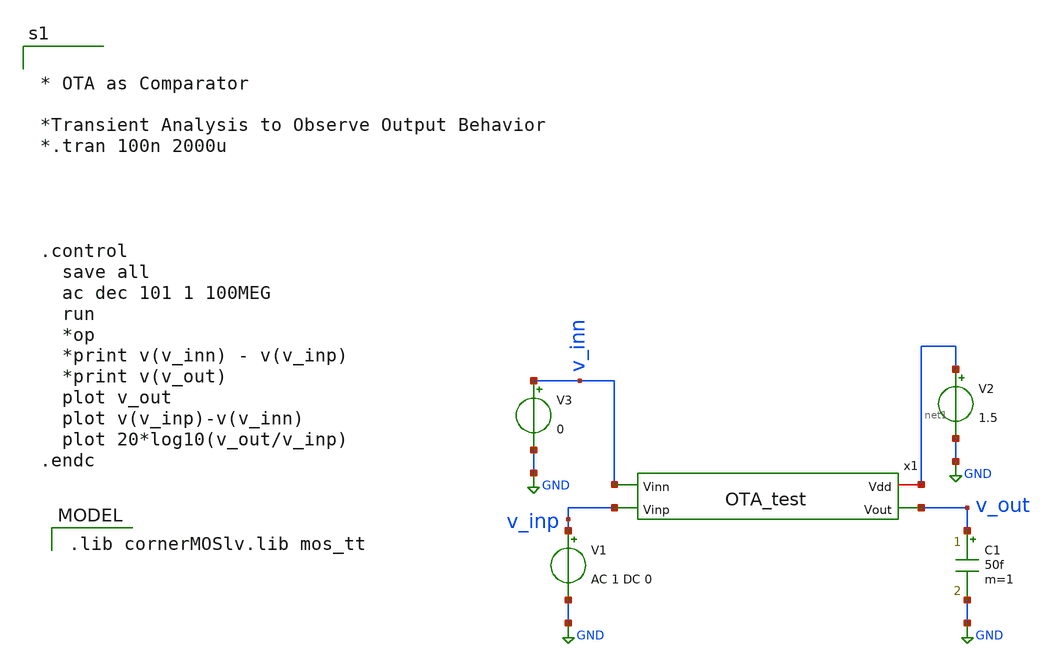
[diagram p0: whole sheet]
** sch_path: Xschem/AC_Analysis.sch
**.subckt AC_Analysis
x1 net1 v_out v_inn v_inp OTA_test
V1 v_inp GND AC 1 DC 0
V2 net1 GND 1.5
C1 v_out GND 50f m=1
V3 v_inn GND 0
**** begin user architecture code


* OTA as Comparator

*Transient Analysis to Observe Output Behavior
*.tran 100n 2000u




.control
  save all
  ac dec 101 1 100MEG
  run
  *op
  *print v(v_inn) - v(v_inp)
  *print v(v_out)
  plot v_out
  plot v(v_inp)-v(v_inn)
  plot 20*log10(v_out/v_inp)
.endc




 .lib cornerMOSlv.lib mos_tt

**** end user architecture code
**.ends

* expanding   symbol:  OTA_test.sym # of pins=4
** sym_path: Xschem/OTA_test.sym
** sch_path: Xschem/OTA_test.sch
.subckt OTA_test Vdd Vout Vinn Vinp
*.opin Vout
*.iopin Vdd
*.ipin Vinp
*.ipin Vinn
I_basis Vdd net3 20u
XM1 net1 Vinp net2 GND sg13_lv_nmos w=2u l=5u ng=1 m=1 mm_ok=1
XM5 net2 net3 GND GND sg13_lv_nmos w=0.5u l=5u ng=1 m=1 mm_ok=1
XM6 net3 net3 GND GND sg13_lv_nmos w=2.5u l=5u ng=5 m=1 mm_ok=1
XM4 Vout net1 Vdd Vdd sg13_lv_pmos w=1.5u l=5u ng=1 m=1 mm_ok=1
XM3 net1 net1 Vdd Vdd sg13_lv_pmos w=1.5u l=5u ng=1 m=1 mm_ok=1
XM2 Vout Vinn net2 GND sg13_lv_nmos w=2u l=5u ng=1 m=1 mm_ok=1
.ends

.GLOBAL GND
.end
